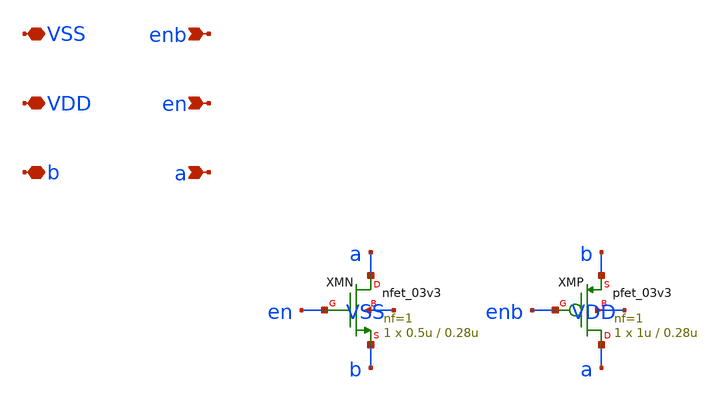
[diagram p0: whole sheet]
** sch_path: design/tg_s.sch
**.subckt tg_s a en enb b VDD VSS
*.ipin a
*.ipin en
*.ipin enb
*.iopin b
*.iopin VDD
*.iopin VSS
XMN a en b VSS nfet_03v3 L=0.28u W=0.5u nf=1 ad='int((nf+1)/2) * W/nf * 0.18u' as='int((nf+2)/2) * W/nf * 0.18u'
+ pd='2*int((nf+1)/2) * (W/nf + 0.18u)' ps='2*int((nf+2)/2) * (W/nf + 0.18u)' nrd='0.18u / W' nrs='0.18u / W'
+ sa=0 sb=0 sd=0 m=1
XMP a enb b VDD pfet_03v3 L=0.28u W=1u nf=1 ad='int((nf+1)/2) * W/nf * 0.18u' as='int((nf+2)/2) * W/nf * 0.18u'
+ pd='2*int((nf+1)/2) * (W/nf + 0.18u)' ps='2*int((nf+2)/2) * (W/nf + 0.18u)' nrd='0.18u / W' nrs='0.18u / W'
+ sa=0 sb=0 sd=0 m=1
**.ends
.end
